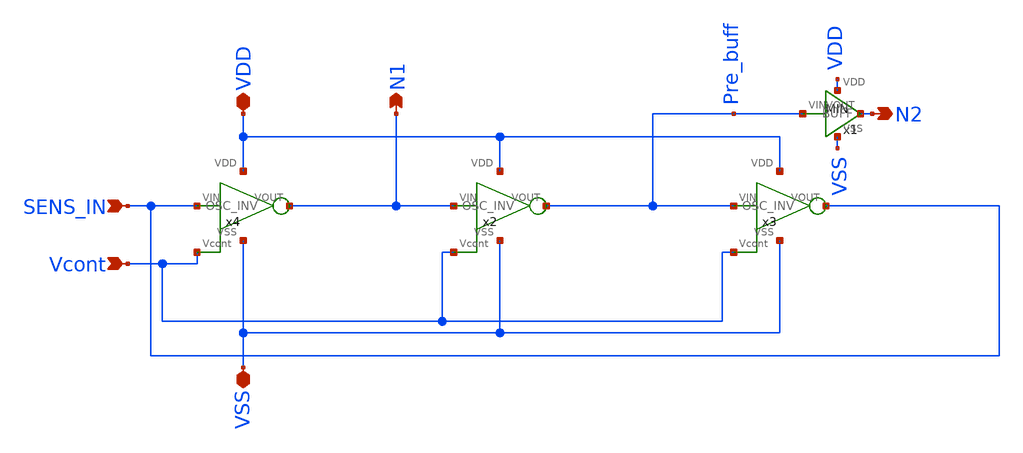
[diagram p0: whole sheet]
** sch_path: ABC123_SDC/design_data/xschem/OSC_RING/OSC_RING.sch
**.subckt OSC_RING SENS_IN VDD VSS N1 N2 Vcont
*.ipin SENS_IN
*.iopin VDD
*.iopin VSS
*.opin N1
*.opin N2
*.ipin Vcont
x1 Pre_buff N2 VDD VSS BUFF
x4 VDD SENS_IN N1 VSS Vcont OSC_INV
x2 VDD N1 Pre_buff VSS Vcont OSC_INV
x3 VDD Pre_buff SENS_IN VSS Vcont OSC_INV
**.ends
.end
